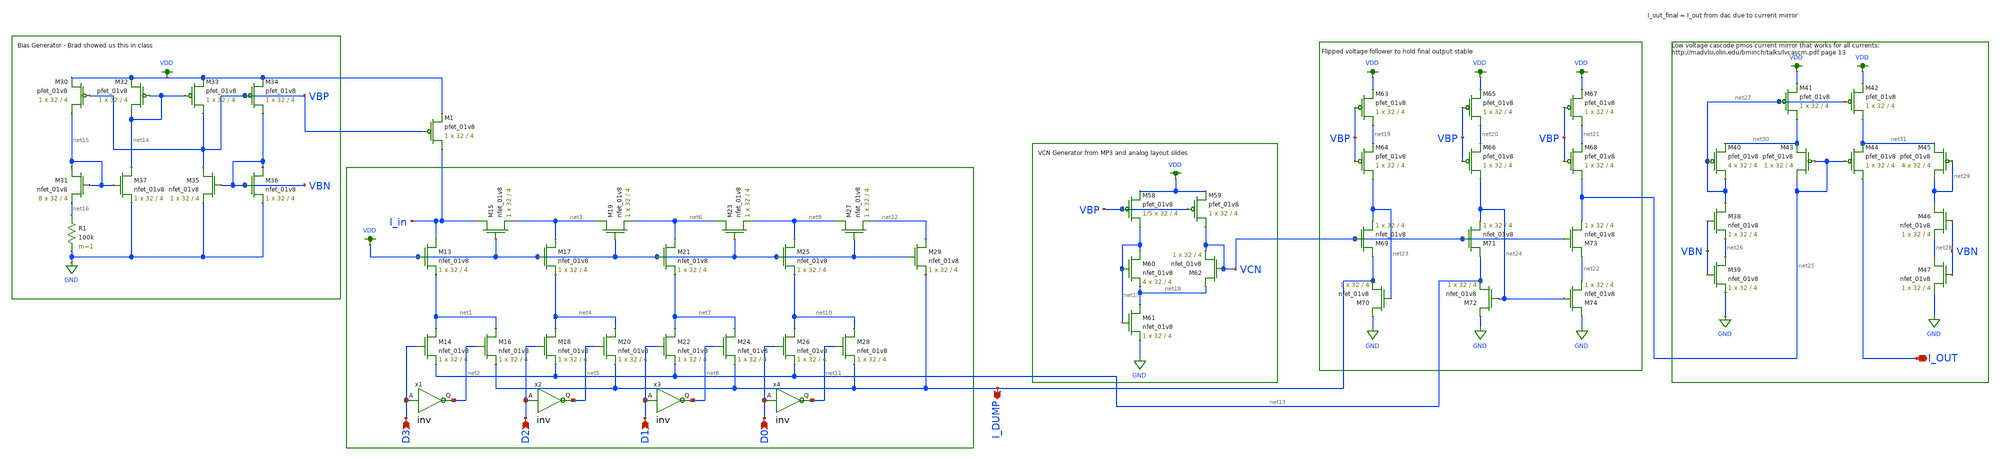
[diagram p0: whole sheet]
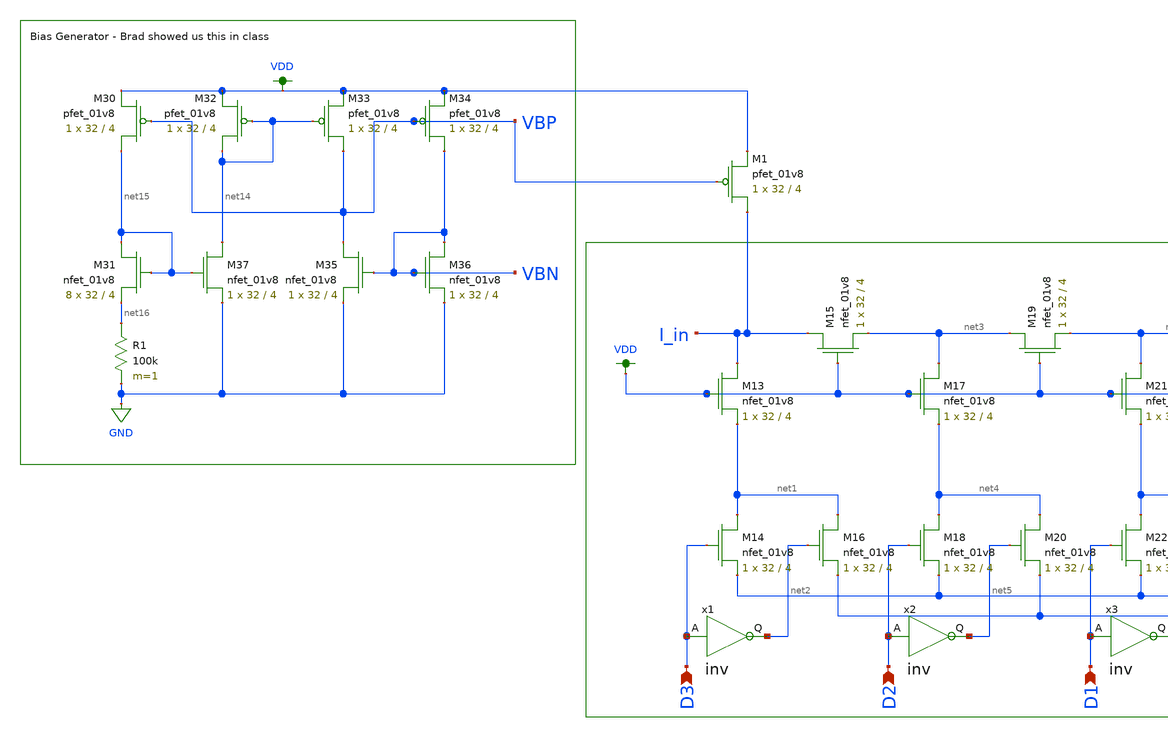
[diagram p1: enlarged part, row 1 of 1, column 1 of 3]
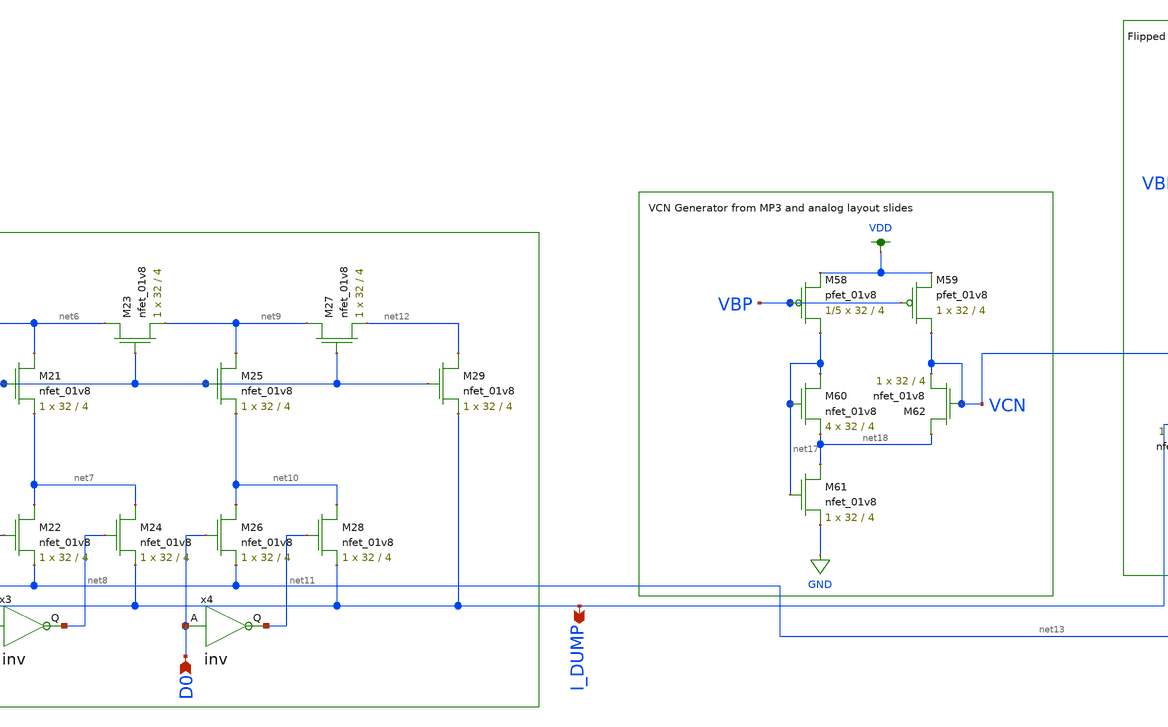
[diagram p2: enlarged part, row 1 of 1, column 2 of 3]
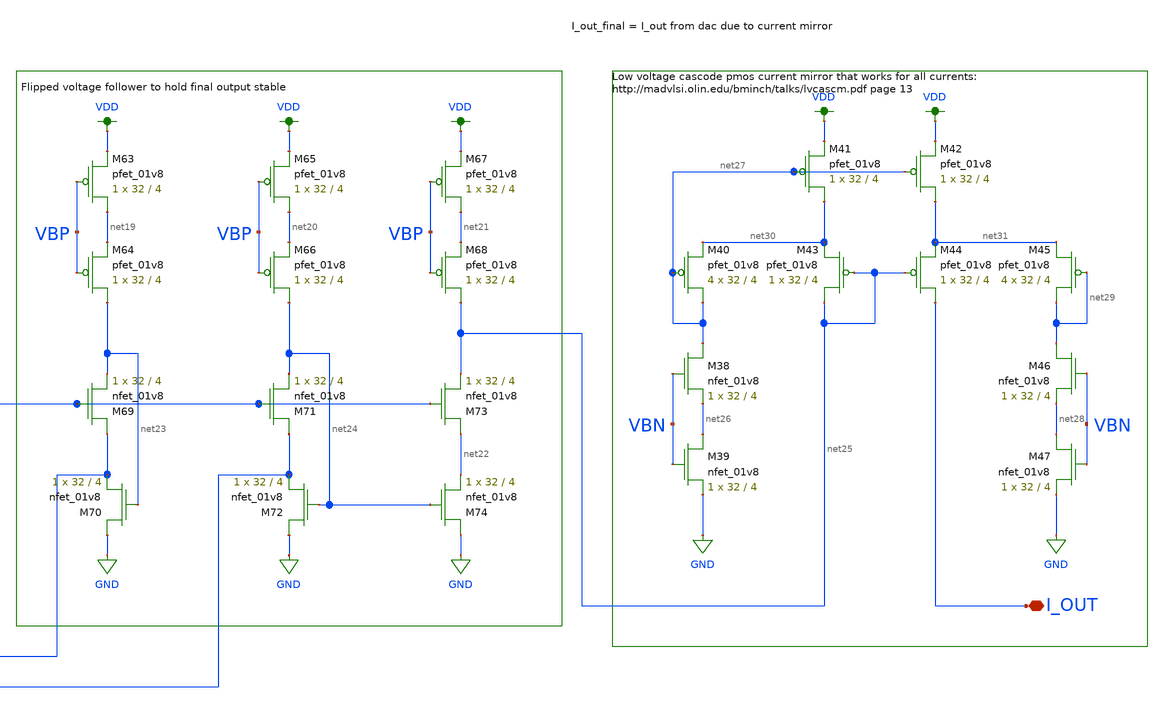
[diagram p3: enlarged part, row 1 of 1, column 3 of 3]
** sch_path: schemas/4BIT_DAC.sch
**.subckt 4BIT_DAC D3 D2 D1 D0 I_DUMP I_OUT
*.ipin D3
*.ipin D2
*.ipin D1
*.ipin D0
*.opin I_DUMP
*.iopin I_OUT
XM13 I_in VDD net1 GND sky130_fd_pr__nfet_01v8 L=4 W=32 nf=1 ad='int((nf+1)/2) * W/nf * 0.29' as='int((nf+2)/2) * W/nf * 0.29'
+ pd='2*int((nf+1)/2) * (W/nf + 0.29)' ps='2*int((nf+2)/2) * (W/nf + 0.29)' nrd='0.29 / W' nrs='0.29 / W'
+ sa=0 sb=0 sd=0 mult=1 m=1
XM14 net1 D3 net13 GND sky130_fd_pr__nfet_01v8 L=4 W=32 nf=1 ad='int((nf+1)/2) * W/nf * 0.29' as='int((nf+2)/2) * W/nf * 0.29'
+ pd='2*int((nf+1)/2) * (W/nf + 0.29)' ps='2*int((nf+2)/2) * (W/nf + 0.29)' nrd='0.29 / W' nrs='0.29 / W'
+ sa=0 sb=0 sd=0 mult=1 m=1
XM15 I_in VDD net3 GND sky130_fd_pr__nfet_01v8 L=4 W=32 nf=1 ad='int((nf+1)/2) * W/nf * 0.29' as='int((nf+2)/2) * W/nf * 0.29'
+ pd='2*int((nf+1)/2) * (W/nf + 0.29)' ps='2*int((nf+2)/2) * (W/nf + 0.29)' nrd='0.29 / W' nrs='0.29 / W'
+ sa=0 sb=0 sd=0 mult=1 m=1
XM16 net1 net2 I_DUMP GND sky130_fd_pr__nfet_01v8 L=4 W=32 nf=1 ad='int((nf+1)/2) * W/nf * 0.29' as='int((nf+2)/2) * W/nf * 0.29'
+ pd='2*int((nf+1)/2) * (W/nf + 0.29)' ps='2*int((nf+2)/2) * (W/nf + 0.29)' nrd='0.29 / W' nrs='0.29 / W'
+ sa=0 sb=0 sd=0 mult=1 m=1
XM17 net3 VDD net4 GND sky130_fd_pr__nfet_01v8 L=4 W=32 nf=1 ad='int((nf+1)/2) * W/nf * 0.29' as='int((nf+2)/2) * W/nf * 0.29'
+ pd='2*int((nf+1)/2) * (W/nf + 0.29)' ps='2*int((nf+2)/2) * (W/nf + 0.29)' nrd='0.29 / W' nrs='0.29 / W'
+ sa=0 sb=0 sd=0 mult=1 m=1
XM18 net4 D2 net13 GND sky130_fd_pr__nfet_01v8 L=4 W=32 nf=1 ad='int((nf+1)/2) * W/nf * 0.29' as='int((nf+2)/2) * W/nf * 0.29'
+ pd='2*int((nf+1)/2) * (W/nf + 0.29)' ps='2*int((nf+2)/2) * (W/nf + 0.29)' nrd='0.29 / W' nrs='0.29 / W'
+ sa=0 sb=0 sd=0 mult=1 m=1
XM19 net3 VDD net6 GND sky130_fd_pr__nfet_01v8 L=4 W=32 nf=1 ad='int((nf+1)/2) * W/nf * 0.29' as='int((nf+2)/2) * W/nf * 0.29'
+ pd='2*int((nf+1)/2) * (W/nf + 0.29)' ps='2*int((nf+2)/2) * (W/nf + 0.29)' nrd='0.29 / W' nrs='0.29 / W'
+ sa=0 sb=0 sd=0 mult=1 m=1
XM20 net4 net5 I_DUMP GND sky130_fd_pr__nfet_01v8 L=4 W=32 nf=1 ad='int((nf+1)/2) * W/nf * 0.29' as='int((nf+2)/2) * W/nf * 0.29'
+ pd='2*int((nf+1)/2) * (W/nf + 0.29)' ps='2*int((nf+2)/2) * (W/nf + 0.29)' nrd='0.29 / W' nrs='0.29 / W'
+ sa=0 sb=0 sd=0 mult=1 m=1
XM21 net6 VDD net7 GND sky130_fd_pr__nfet_01v8 L=4 W=32 nf=1 ad='int((nf+1)/2) * W/nf * 0.29' as='int((nf+2)/2) * W/nf * 0.29'
+ pd='2*int((nf+1)/2) * (W/nf + 0.29)' ps='2*int((nf+2)/2) * (W/nf + 0.29)' nrd='0.29 / W' nrs='0.29 / W'
+ sa=0 sb=0 sd=0 mult=1 m=1
XM22 net7 D1 net13 GND sky130_fd_pr__nfet_01v8 L=4 W=32 nf=1 ad='int((nf+1)/2) * W/nf * 0.29' as='int((nf+2)/2) * W/nf * 0.29'
+ pd='2*int((nf+1)/2) * (W/nf + 0.29)' ps='2*int((nf+2)/2) * (W/nf + 0.29)' nrd='0.29 / W' nrs='0.29 / W'
+ sa=0 sb=0 sd=0 mult=1 m=1
XM23 net6 VDD net9 GND sky130_fd_pr__nfet_01v8 L=4 W=32 nf=1 ad='int((nf+1)/2) * W/nf * 0.29' as='int((nf+2)/2) * W/nf * 0.29'
+ pd='2*int((nf+1)/2) * (W/nf + 0.29)' ps='2*int((nf+2)/2) * (W/nf + 0.29)' nrd='0.29 / W' nrs='0.29 / W'
+ sa=0 sb=0 sd=0 mult=1 m=1
XM24 net7 net8 I_DUMP GND sky130_fd_pr__nfet_01v8 L=4 W=32 nf=1 ad='int((nf+1)/2) * W/nf * 0.29' as='int((nf+2)/2) * W/nf * 0.29'
+ pd='2*int((nf+1)/2) * (W/nf + 0.29)' ps='2*int((nf+2)/2) * (W/nf + 0.29)' nrd='0.29 / W' nrs='0.29 / W'
+ sa=0 sb=0 sd=0 mult=1 m=1
XM25 net9 VDD net10 GND sky130_fd_pr__nfet_01v8 L=4 W=32 nf=1 ad='int((nf+1)/2) * W/nf * 0.29' as='int((nf+2)/2) * W/nf * 0.29'
+ pd='2*int((nf+1)/2) * (W/nf + 0.29)' ps='2*int((nf+2)/2) * (W/nf + 0.29)' nrd='0.29 / W' nrs='0.29 / W'
+ sa=0 sb=0 sd=0 mult=1 m=1
XM26 net10 D0 net13 GND sky130_fd_pr__nfet_01v8 L=4 W=32 nf=1 ad='int((nf+1)/2) * W/nf * 0.29' as='int((nf+2)/2) * W/nf * 0.29'
+ pd='2*int((nf+1)/2) * (W/nf + 0.29)' ps='2*int((nf+2)/2) * (W/nf + 0.29)' nrd='0.29 / W' nrs='0.29 / W'
+ sa=0 sb=0 sd=0 mult=1 m=1
XM27 net9 VDD net12 GND sky130_fd_pr__nfet_01v8 L=4 W=32 nf=1 ad='int((nf+1)/2) * W/nf * 0.29' as='int((nf+2)/2) * W/nf * 0.29'
+ pd='2*int((nf+1)/2) * (W/nf + 0.29)' ps='2*int((nf+2)/2) * (W/nf + 0.29)' nrd='0.29 / W' nrs='0.29 / W'
+ sa=0 sb=0 sd=0 mult=1 m=1
XM28 net10 net11 I_DUMP GND sky130_fd_pr__nfet_01v8 L=4 W=32 nf=1 ad='int((nf+1)/2) * W/nf * 0.29' as='int((nf+2)/2) * W/nf * 0.29'
+ pd='2*int((nf+1)/2) * (W/nf + 0.29)' ps='2*int((nf+2)/2) * (W/nf + 0.29)' nrd='0.29 / W' nrs='0.29 / W'
+ sa=0 sb=0 sd=0 mult=1 m=1
XM29 net12 VDD I_DUMP GND sky130_fd_pr__nfet_01v8 L=4 W=32 nf=1 ad='int((nf+1)/2) * W/nf * 0.29' as='int((nf+2)/2) * W/nf * 0.29'
+ pd='2*int((nf+1)/2) * (W/nf + 0.29)' ps='2*int((nf+2)/2) * (W/nf + 0.29)' nrd='0.29 / W' nrs='0.29 / W'
+ sa=0 sb=0 sd=0 mult=1 m=1
XM30 net15 VBP VDD VDD sky130_fd_pr__pfet_01v8 L=4 W=32 nf=1 ad='int((nf+1)/2) * W/nf * 0.29' as='int((nf+2)/2) * W/nf * 0.29'
+ pd='2*int((nf+1)/2) * (W/nf + 0.29)' ps='2*int((nf+2)/2) * (W/nf + 0.29)' nrd='0.29 / W' nrs='0.29 / W'
+ sa=0 sb=0 sd=0 mult=1 m=1
XM31 net15 net15 net16 GND sky130_fd_pr__nfet_01v8 L=4 W=32 nf=1 ad='int((nf+1)/2) * W/nf * 0.29' as='int((nf+2)/2) * W/nf * 0.29'
+ pd='2*int((nf+1)/2) * (W/nf + 0.29)' ps='2*int((nf+2)/2) * (W/nf + 0.29)' nrd='0.29 / W' nrs='0.29 / W'
+ sa=0 sb=0 sd=0 mult=8 m=8
XM32 net14 net14 VDD VDD sky130_fd_pr__pfet_01v8 L=4 W=32 nf=1 ad='int((nf+1)/2) * W/nf * 0.29' as='int((nf+2)/2) * W/nf * 0.29'
+ pd='2*int((nf+1)/2) * (W/nf + 0.29)' ps='2*int((nf+2)/2) * (W/nf + 0.29)' nrd='0.29 / W' nrs='0.29 / W'
+ sa=0 sb=0 sd=0 mult=1 m=1
XM33 VBP net14 VDD VDD sky130_fd_pr__pfet_01v8 L=4 W=32 nf=1 ad='int((nf+1)/2) * W/nf * 0.29' as='int((nf+2)/2) * W/nf * 0.29'
+ pd='2*int((nf+1)/2) * (W/nf + 0.29)' ps='2*int((nf+2)/2) * (W/nf + 0.29)' nrd='0.29 / W' nrs='0.29 / W'
+ sa=0 sb=0 sd=0 mult=1 m=1
XM34 VBN VBP VDD VDD sky130_fd_pr__pfet_01v8 L=4 W=32 nf=1 ad='int((nf+1)/2) * W/nf * 0.29' as='int((nf+2)/2) * W/nf * 0.29'
+ pd='2*int((nf+1)/2) * (W/nf + 0.29)' ps='2*int((nf+2)/2) * (W/nf + 0.29)' nrd='0.29 / W' nrs='0.29 / W'
+ sa=0 sb=0 sd=0 mult=1 m=1
XM35 VBP VBN GND GND sky130_fd_pr__nfet_01v8 L=4 W=32 nf=1 ad='int((nf+1)/2) * W/nf * 0.29' as='int((nf+2)/2) * W/nf * 0.29'
+ pd='2*int((nf+1)/2) * (W/nf + 0.29)' ps='2*int((nf+2)/2) * (W/nf + 0.29)' nrd='0.29 / W' nrs='0.29 / W'
+ sa=0 sb=0 sd=0 mult=1 m=1
XM36 VBN VBN GND GND sky130_fd_pr__nfet_01v8 L=4 W=32 nf=1 ad='int((nf+1)/2) * W/nf * 0.29' as='int((nf+2)/2) * W/nf * 0.29'
+ pd='2*int((nf+1)/2) * (W/nf + 0.29)' ps='2*int((nf+2)/2) * (W/nf + 0.29)' nrd='0.29 / W' nrs='0.29 / W'
+ sa=0 sb=0 sd=0 mult=1 m=1
XM37 net14 net15 GND GND sky130_fd_pr__nfet_01v8 L=4 W=32 nf=1 ad='int((nf+1)/2) * W/nf * 0.29' as='int((nf+2)/2) * W/nf * 0.29'
+ pd='2*int((nf+1)/2) * (W/nf + 0.29)' ps='2*int((nf+2)/2) * (W/nf + 0.29)' nrd='0.29 / W' nrs='0.29 / W'
+ sa=0 sb=0 sd=0 mult=1 m=1
R1 net16 GND 100k m=1
XM58 net17 VBP VDD VDD sky130_fd_pr__pfet_01v8 L=4 W=32 nf=1 ad='int((nf+1)/2) * W/nf * 0.29' as='int((nf+2)/2) * W/nf * 0.29'
+ pd='2*int((nf+1)/2) * (W/nf + 0.29)' ps='2*int((nf+2)/2) * (W/nf + 0.29)' nrd='0.29 / W' nrs='0.29 / W'
+ sa=0 sb=0 sd=0 mult=1/5 m=1/5
XM59 VCN VBP VDD VDD sky130_fd_pr__pfet_01v8 L=4 W=32 nf=1 ad='int((nf+1)/2) * W/nf * 0.29' as='int((nf+2)/2) * W/nf * 0.29'
+ pd='2*int((nf+1)/2) * (W/nf + 0.29)' ps='2*int((nf+2)/2) * (W/nf + 0.29)' nrd='0.29 / W' nrs='0.29 / W'
+ sa=0 sb=0 sd=0 mult=1 m=1
XM60 net17 net17 net18 GND sky130_fd_pr__nfet_01v8 L=4 W=32 nf=1 ad='int((nf+1)/2) * W/nf * 0.29' as='int((nf+2)/2) * W/nf * 0.29'
+ pd='2*int((nf+1)/2) * (W/nf + 0.29)' ps='2*int((nf+2)/2) * (W/nf + 0.29)' nrd='0.29 / W' nrs='0.29 / W'
+ sa=0 sb=0 sd=0 mult=4 m=4
XM61 net18 net17 GND GND sky130_fd_pr__nfet_01v8 L=4 W=32 nf=1 ad='int((nf+1)/2) * W/nf * 0.29' as='int((nf+2)/2) * W/nf * 0.29'
+ pd='2*int((nf+1)/2) * (W/nf + 0.29)' ps='2*int((nf+2)/2) * (W/nf + 0.29)' nrd='0.29 / W' nrs='0.29 / W'
+ sa=0 sb=0 sd=0 mult=1 m=1
XM62 net18 VCN VCN GND sky130_fd_pr__nfet_01v8 L=4 W=32 nf=1 ad='int((nf+1)/2) * W/nf * 0.29' as='int((nf+2)/2) * W/nf * 0.29'
+ pd='2*int((nf+1)/2) * (W/nf + 0.29)' ps='2*int((nf+2)/2) * (W/nf + 0.29)' nrd='0.29 / W' nrs='0.29 / W'
+ sa=0 sb=0 sd=0 mult=1 m=1
XM63 net19 VBP VDD VDD sky130_fd_pr__pfet_01v8 L=4 W=32 nf=1 ad='int((nf+1)/2) * W/nf * 0.29' as='int((nf+2)/2) * W/nf * 0.29'
+ pd='2*int((nf+1)/2) * (W/nf + 0.29)' ps='2*int((nf+2)/2) * (W/nf + 0.29)' nrd='0.29 / W' nrs='0.29 / W'
+ sa=0 sb=0 sd=0 mult=1 m=1
XM64 net23 VBP net19 VDD sky130_fd_pr__pfet_01v8 L=4 W=32 nf=1 ad='int((nf+1)/2) * W/nf * 0.29' as='int((nf+2)/2) * W/nf * 0.29'
+ pd='2*int((nf+1)/2) * (W/nf + 0.29)' ps='2*int((nf+2)/2) * (W/nf + 0.29)' nrd='0.29 / W' nrs='0.29 / W'
+ sa=0 sb=0 sd=0 mult=1 m=1
XM65 net20 VBP VDD VDD sky130_fd_pr__pfet_01v8 L=4 W=32 nf=1 ad='int((nf+1)/2) * W/nf * 0.29' as='int((nf+2)/2) * W/nf * 0.29'
+ pd='2*int((nf+1)/2) * (W/nf + 0.29)' ps='2*int((nf+2)/2) * (W/nf + 0.29)' nrd='0.29 / W' nrs='0.29 / W'
+ sa=0 sb=0 sd=0 mult=1 m=1
XM66 net24 VBP net20 VDD sky130_fd_pr__pfet_01v8 L=4 W=32 nf=1 ad='int((nf+1)/2) * W/nf * 0.29' as='int((nf+2)/2) * W/nf * 0.29'
+ pd='2*int((nf+1)/2) * (W/nf + 0.29)' ps='2*int((nf+2)/2) * (W/nf + 0.29)' nrd='0.29 / W' nrs='0.29 / W'
+ sa=0 sb=0 sd=0 mult=1 m=1
XM67 net21 VBP VDD VDD sky130_fd_pr__pfet_01v8 L=4 W=32 nf=1 ad='int((nf+1)/2) * W/nf * 0.29' as='int((nf+2)/2) * W/nf * 0.29'
+ pd='2*int((nf+1)/2) * (W/nf + 0.29)' ps='2*int((nf+2)/2) * (W/nf + 0.29)' nrd='0.29 / W' nrs='0.29 / W'
+ sa=0 sb=0 sd=0 mult=1 m=1
XM68 net25 VBP net21 VDD sky130_fd_pr__pfet_01v8 L=4 W=32 nf=1 ad='int((nf+1)/2) * W/nf * 0.29' as='int((nf+2)/2) * W/nf * 0.29'
+ pd='2*int((nf+1)/2) * (W/nf + 0.29)' ps='2*int((nf+2)/2) * (W/nf + 0.29)' nrd='0.29 / W' nrs='0.29 / W'
+ sa=0 sb=0 sd=0 mult=1 m=1
XM69 I_DUMP VCN net23 GND sky130_fd_pr__nfet_01v8 L=4 W=32 nf=1 ad='int((nf+1)/2) * W/nf * 0.29' as='int((nf+2)/2) * W/nf * 0.29'
+ pd='2*int((nf+1)/2) * (W/nf + 0.29)' ps='2*int((nf+2)/2) * (W/nf + 0.29)' nrd='0.29 / W' nrs='0.29 / W'
+ sa=0 sb=0 sd=0 mult=1 m=1
XM70 GND net23 I_DUMP GND sky130_fd_pr__nfet_01v8 L=4 W=32 nf=1 ad='int((nf+1)/2) * W/nf * 0.29' as='int((nf+2)/2) * W/nf * 0.29'
+ pd='2*int((nf+1)/2) * (W/nf + 0.29)' ps='2*int((nf+2)/2) * (W/nf + 0.29)' nrd='0.29 / W' nrs='0.29 / W'
+ sa=0 sb=0 sd=0 mult=1 m=1
XM71 net13 VCN net24 GND sky130_fd_pr__nfet_01v8 L=4 W=32 nf=1 ad='int((nf+1)/2) * W/nf * 0.29' as='int((nf+2)/2) * W/nf * 0.29'
+ pd='2*int((nf+1)/2) * (W/nf + 0.29)' ps='2*int((nf+2)/2) * (W/nf + 0.29)' nrd='0.29 / W' nrs='0.29 / W'
+ sa=0 sb=0 sd=0 mult=1 m=1
XM72 GND net24 net13 GND sky130_fd_pr__nfet_01v8 L=4 W=32 nf=1 ad='int((nf+1)/2) * W/nf * 0.29' as='int((nf+2)/2) * W/nf * 0.29'
+ pd='2*int((nf+1)/2) * (W/nf + 0.29)' ps='2*int((nf+2)/2) * (W/nf + 0.29)' nrd='0.29 / W' nrs='0.29 / W'
+ sa=0 sb=0 sd=0 mult=1 m=1
XM73 net22 VCN net25 GND sky130_fd_pr__nfet_01v8 L=4 W=32 nf=1 ad='int((nf+1)/2) * W/nf * 0.29' as='int((nf+2)/2) * W/nf * 0.29'
+ pd='2*int((nf+1)/2) * (W/nf + 0.29)' ps='2*int((nf+2)/2) * (W/nf + 0.29)' nrd='0.29 / W' nrs='0.29 / W'
+ sa=0 sb=0 sd=0 mult=1 m=1
XM74 GND net24 net22 GND sky130_fd_pr__nfet_01v8 L=4 W=32 nf=1 ad='int((nf+1)/2) * W/nf * 0.29' as='int((nf+2)/2) * W/nf * 0.29'
+ pd='2*int((nf+1)/2) * (W/nf + 0.29)' ps='2*int((nf+2)/2) * (W/nf + 0.29)' nrd='0.29 / W' nrs='0.29 / W'
+ sa=0 sb=0 sd=0 mult=1 m=1
x1 net2 D3 inv
x2 net5 D2 inv
x3 net8 D1 inv
x4 net11 D0 inv
XM1 I_in VBP VDD VDD sky130_fd_pr__pfet_01v8 L=4 W=32 nf=1 ad='int((nf+1)/2) * W/nf * 0.29' as='int((nf+2)/2) * W/nf * 0.29'
+ pd='2*int((nf+1)/2) * (W/nf + 0.29)' ps='2*int((nf+2)/2) * (W/nf + 0.29)' nrd='0.29 / W' nrs='0.29 / W'
+ sa=0 sb=0 sd=0 mult=1 m=1
XM38 net27 VBN net26 GND sky130_fd_pr__nfet_01v8 L=4 W=32 nf=1 ad='int((nf+1)/2) * W/nf * 0.29' as='int((nf+2)/2) * W/nf * 0.29'
+ pd='2*int((nf+1)/2) * (W/nf + 0.29)' ps='2*int((nf+2)/2) * (W/nf + 0.29)' nrd='0.29 / W' nrs='0.29 / W'
+ sa=0 sb=0 sd=0 mult=1 m=1
XM39 net26 VBN GND GND sky130_fd_pr__nfet_01v8 L=4 W=32 nf=1 ad='int((nf+1)/2) * W/nf * 0.29' as='int((nf+2)/2) * W/nf * 0.29'
+ pd='2*int((nf+1)/2) * (W/nf + 0.29)' ps='2*int((nf+2)/2) * (W/nf + 0.29)' nrd='0.29 / W' nrs='0.29 / W'
+ sa=0 sb=0 sd=0 mult=1 m=1
XM40 net27 net27 net30 VDD sky130_fd_pr__pfet_01v8 L=4 W=32 nf=1 ad='int((nf+1)/2) * W/nf * 0.29' as='int((nf+2)/2) * W/nf * 0.29'
+ pd='2*int((nf+1)/2) * (W/nf + 0.29)' ps='2*int((nf+2)/2) * (W/nf + 0.29)' nrd='0.29 / W' nrs='0.29 / W'
+ sa=0 sb=0 sd=0 mult=4 m=4
XM41 net30 net27 VDD VDD sky130_fd_pr__pfet_01v8 L=4 W=32 nf=1 ad='int((nf+1)/2) * W/nf * 0.29' as='int((nf+2)/2) * W/nf * 0.29'
+ pd='2*int((nf+1)/2) * (W/nf + 0.29)' ps='2*int((nf+2)/2) * (W/nf + 0.29)' nrd='0.29 / W' nrs='0.29 / W'
+ sa=0 sb=0 sd=0 mult=1 m=1
XM42 net31 net27 VDD VDD sky130_fd_pr__pfet_01v8 L=4 W=32 nf=1 ad='int((nf+1)/2) * W/nf * 0.29' as='int((nf+2)/2) * W/nf * 0.29'
+ pd='2*int((nf+1)/2) * (W/nf + 0.29)' ps='2*int((nf+2)/2) * (W/nf + 0.29)' nrd='0.29 / W' nrs='0.29 / W'
+ sa=0 sb=0 sd=0 mult=1 m=1
XM43 net25 net25 net30 VDD sky130_fd_pr__pfet_01v8 L=4 W=32 nf=1 ad='int((nf+1)/2) * W/nf * 0.29' as='int((nf+2)/2) * W/nf * 0.29'
+ pd='2*int((nf+1)/2) * (W/nf + 0.29)' ps='2*int((nf+2)/2) * (W/nf + 0.29)' nrd='0.29 / W' nrs='0.29 / W'
+ sa=0 sb=0 sd=0 mult=1 m=1
XM44 I_OUT net25 net31 VDD sky130_fd_pr__pfet_01v8 L=4 W=32 nf=1 ad='int((nf+1)/2) * W/nf * 0.29' as='int((nf+2)/2) * W/nf * 0.29'
+ pd='2*int((nf+1)/2) * (W/nf + 0.29)' ps='2*int((nf+2)/2) * (W/nf + 0.29)' nrd='0.29 / W' nrs='0.29 / W'
+ sa=0 sb=0 sd=0 mult=1 m=1
XM45 net29 net29 net31 VDD sky130_fd_pr__pfet_01v8 L=4 W=32 nf=1 ad='int((nf+1)/2) * W/nf * 0.29' as='int((nf+2)/2) * W/nf * 0.29'
+ pd='2*int((nf+1)/2) * (W/nf + 0.29)' ps='2*int((nf+2)/2) * (W/nf + 0.29)' nrd='0.29 / W' nrs='0.29 / W'
+ sa=0 sb=0 sd=0 mult=4 m=4
XM46 net29 VBN net28 GND sky130_fd_pr__nfet_01v8 L=4 W=32 nf=1 ad='int((nf+1)/2) * W/nf * 0.29' as='int((nf+2)/2) * W/nf * 0.29'
+ pd='2*int((nf+1)/2) * (W/nf + 0.29)' ps='2*int((nf+2)/2) * (W/nf + 0.29)' nrd='0.29 / W' nrs='0.29 / W'
+ sa=0 sb=0 sd=0 mult=1 m=1
XM47 net28 VBN GND GND sky130_fd_pr__nfet_01v8 L=4 W=32 nf=1 ad='int((nf+1)/2) * W/nf * 0.29' as='int((nf+2)/2) * W/nf * 0.29'
+ pd='2*int((nf+1)/2) * (W/nf + 0.29)' ps='2*int((nf+2)/2) * (W/nf + 0.29)' nrd='0.29 / W' nrs='0.29 / W'
+ sa=0 sb=0 sd=0 mult=1 m=1
**.ends

* expanding   symbol:  /home/mstopyra/Documents/DTILO/schemas/inv.sym # of pins=2
** sym_path: schemas/inv.sym
** sch_path: schemas/inv.sch
.subckt inv Q A
*.ipin A
*.opin Q
XM1 Q A GND GND sky130_fd_pr__nfet_01v8 L=0.15 W=1 nf=1 ad='int((nf+1)/2) * W/nf * 0.29' as='int((nf+2)/2) * W/nf * 0.29'
+ pd='2*int((nf+1)/2) * (W/nf + 0.29)' ps='2*int((nf+2)/2) * (W/nf + 0.29)' nrd='0.29 / W' nrs='0.29 / W'
+ sa=0 sb=0 sd=0 mult=1 m=1
XM2 Q A VDD VDD sky130_fd_pr__pfet_01v8 L=0.15 W=1 nf=1 ad='int((nf+1)/2) * W/nf * 0.29' as='int((nf+2)/2) * W/nf * 0.29'
+ pd='2*int((nf+1)/2) * (W/nf + 0.29)' ps='2*int((nf+2)/2) * (W/nf + 0.29)' nrd='0.29 / W' nrs='0.29 / W'
+ sa=0 sb=0 sd=0 mult=1 m=1
.ends

.GLOBAL GND
.GLOBAL VDD
.end
